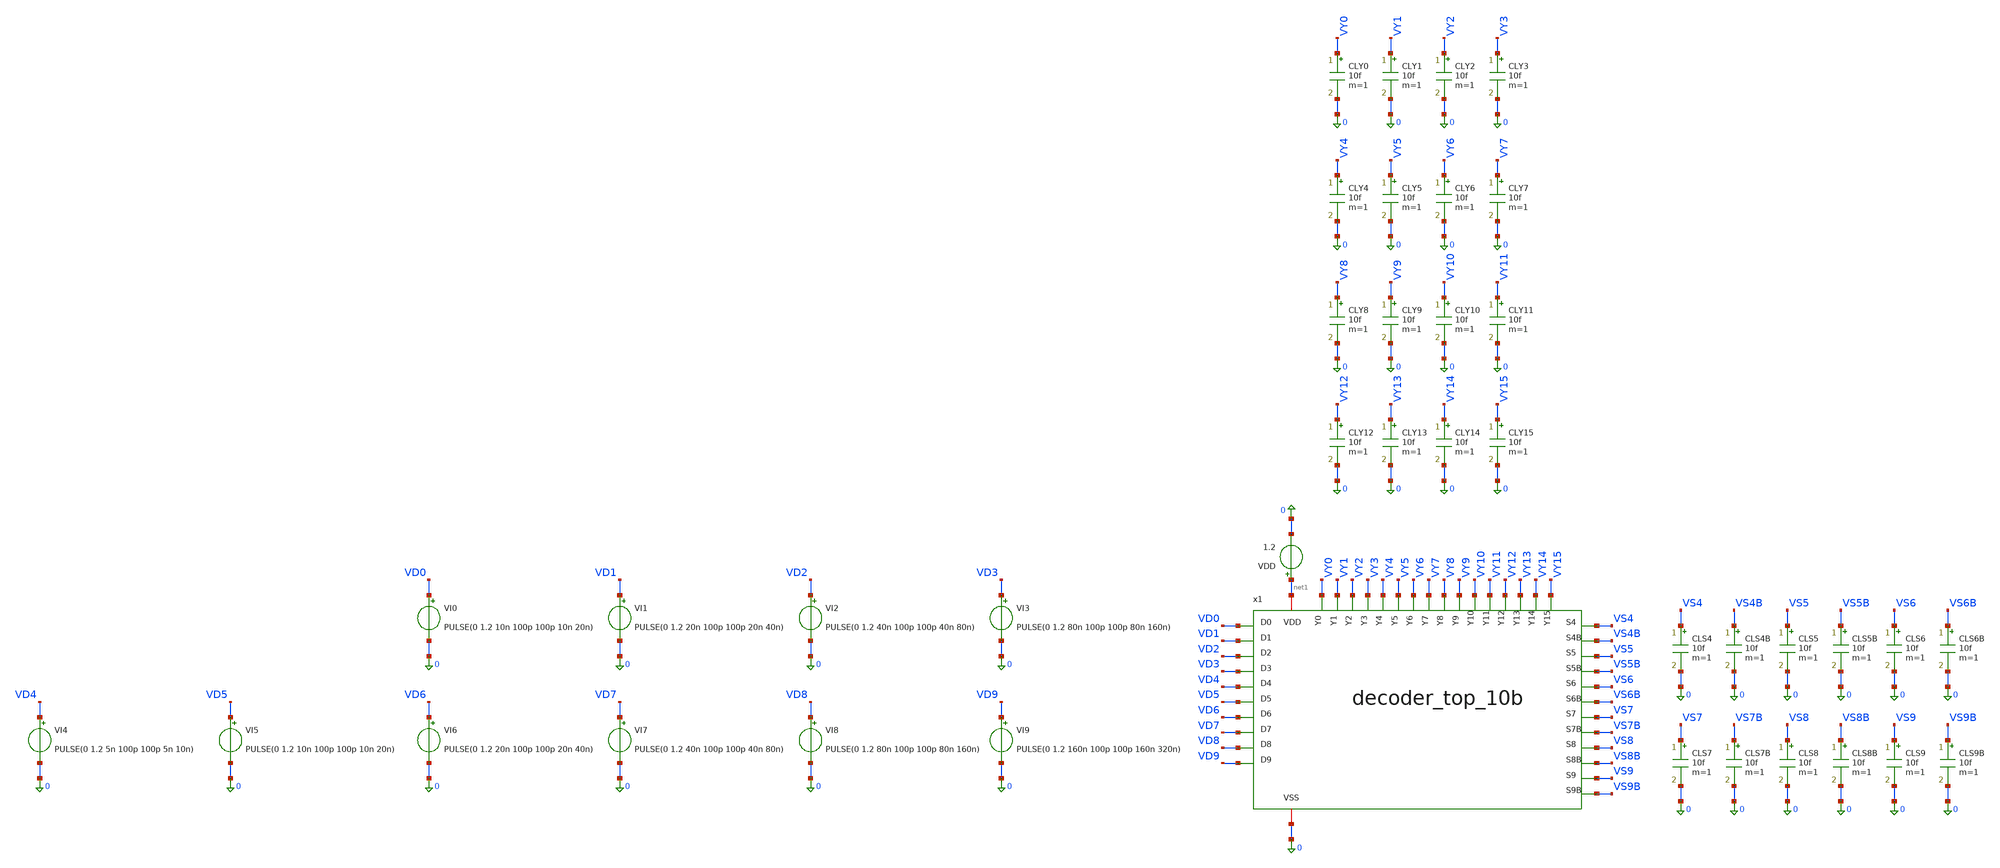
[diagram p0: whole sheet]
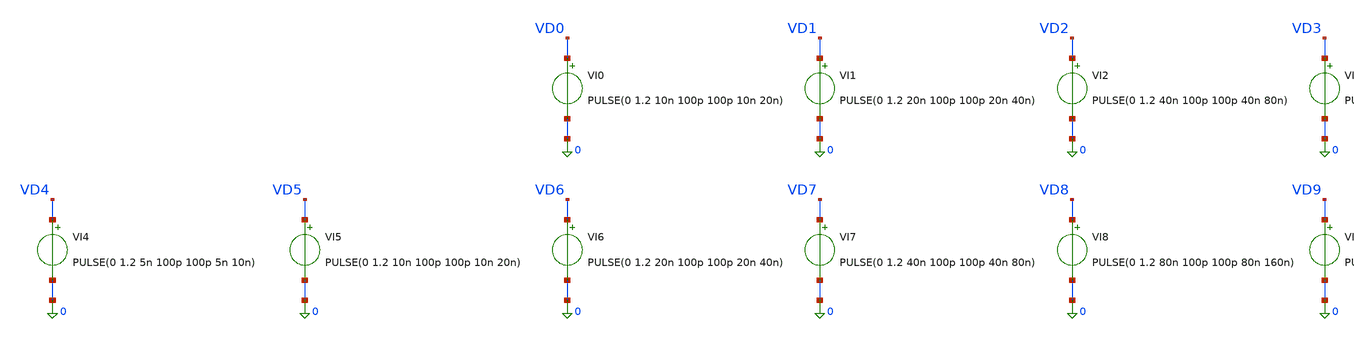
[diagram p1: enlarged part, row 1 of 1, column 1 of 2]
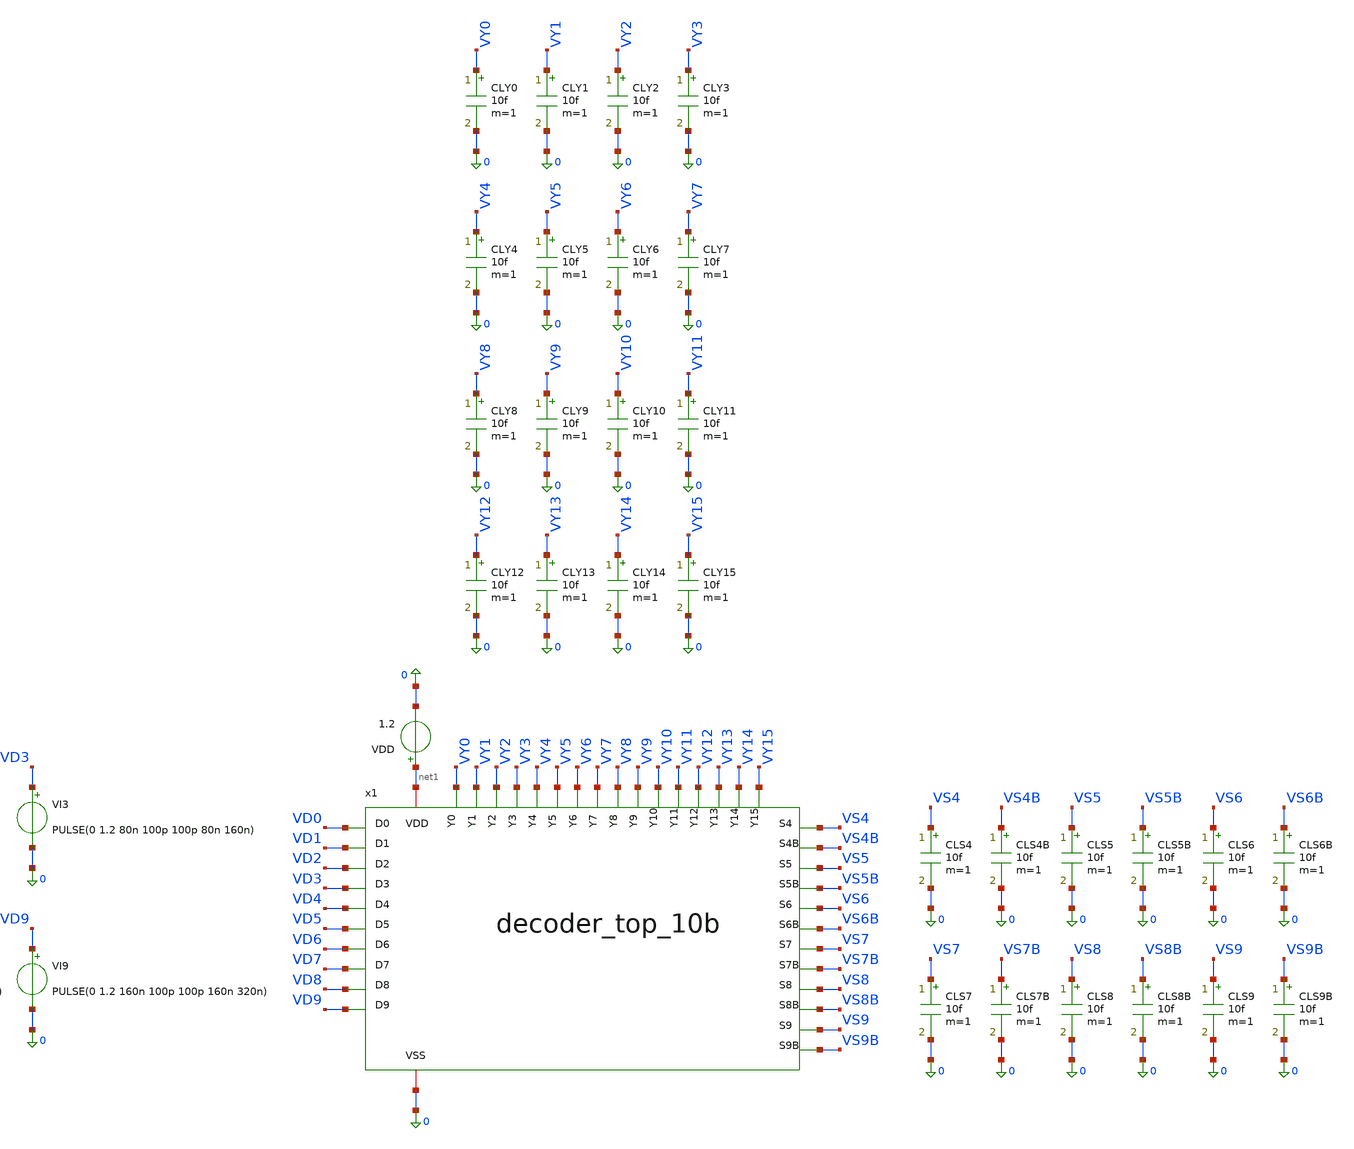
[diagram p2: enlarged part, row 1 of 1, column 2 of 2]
** sch_path: designs/archives/decoder_top_10b/tb_decoder_top_10b.sch
**.subckt tb_decoder_top_10b
x1 VD0 VD3 VY0 VY1 VY2 VY3 net1 0 VY4 VY5 VY6 VY7 VY8 VY9 VY10 VY11 VY12 VY13 VY14 VY15 VD1 VD2 VD4
+ VD7 VD5 VD6 VD8 VD9 VS4 VS4B VS5 VS5B VS6 VS6B VS7 VS7B VS8 VS8B VS9 VS9B decoder_top_10b
VDD net1 0 1.2
VI0 VD0 0 PULSE(0 1.2 10n 100p 100p 10n 20n)
VI1 VD1 0 PULSE(0 1.2 20n 100p 100p 20n 40n)
VI2 VD2 0 PULSE(0 1.2 40n 100p 100p 40n 80n)
VI3 VD3 0 PULSE(0 1.2 80n 100p 100p 80n 160n)
VI4 VD4 0 PULSE(0 1.2 5n 100p 100p 5n 10n)
VI5 VD5 0 PULSE(0 1.2 10n 100p 100p 10n 20n)
VI6 VD6 0 PULSE(0 1.2 20n 100p 100p 20n 40n)
VI7 VD7 0 PULSE(0 1.2 40n 100p 100p 40n 80n)
VI8 VD8 0 PULSE(0 1.2 80n 100p 100p 80n 160n)
VI9 VD9 0 PULSE(0 1.2 160n 100p 100p 160n 320n)
CLY0 VY0 0 10f m=1
CLY1 VY1 0 10f m=1
CLY2 VY2 0 10f m=1
CLY3 VY3 0 10f m=1
CLY4 VY4 0 10f m=1
CLY5 VY5 0 10f m=1
CLY6 VY6 0 10f m=1
CLY7 VY7 0 10f m=1
CLY8 VY8 0 10f m=1
CLY9 VY9 0 10f m=1
CLY10 VY10 0 10f m=1
CLY11 VY11 0 10f m=1
CLY12 VY12 0 10f m=1
CLY13 VY13 0 10f m=1
CLY14 VY14 0 10f m=1
CLY15 VY15 0 10f m=1
CLS4 VS4 0 10f m=1
CLS4B VS4B 0 10f m=1
CLS6B VS6B 0 10f m=1
CLS5B VS5B 0 10f m=1
CLS5 VS5 0 10f m=1
CLS6 VS6 0 10f m=1
CLS7 VS7 0 10f m=1
CLS7B VS7B 0 10f m=1
CLS8 VS8 0 10f m=1
CLS8B VS8B 0 10f m=1
CLS9 VS9 0 10f m=1
CLS9B VS9B 0 10f m=1
**** begin user architecture code

.lib cornerMOSlv.lib mos_tt
.include /foss/pdks/ihp-sg13cmos5l/libs.ref/sg13cmos5l_stdcell/spice/sg13cmos5l_stdcell.spice


.control
  tran 100p 320n
  write tb_decoder_top_10b.raw

  * ==========================================
  * 1. COARSE GAIN STAGE (D0..D3 -> Y0..Y15)
  * ==========================================
  * Coarse 4-bit Binary Inputs (D0..D3)
  plot v(VD0) v(VD1)+1.5 v(VD2)+3.0 v(VD3)+4.5 title 'Coarse Inputs (D0, D1, D2, D3)' xlabel 'Time (s)'
+ ylabel 'Voltage (V)'

  * Coarse Outputs Lower 8 Channels (Y0..Y7)
  plot v(VY0) v(VY1)+1.5 v(VY2)+3.0 v(VY3)+4.5 v(VY4)+6.0 v(VY5)+7.5 v(VY6)+9.0 v(VY7)+10.5 title 'Coarse Decoded Outputs (Y0..Y7)'
+ xlabel 'Time (s)' ylabel 'Voltage (V)'

  * Coarse Outputs Upper 8 Channels (Y8..Y15)
  plot v(VY8) v(VY9)+1.5 v(VY10)+3.0 v(VY11)+4.5 v(VY12)+6.0 v(VY13)+7.5 v(VY14)+9.0 v(VY15)+10.5 title
+ 'Coarse Decoded Outputs (Y8..Y15)' xlabel 'Time (s)' ylabel 'Voltage (V)'

  * ==========================================
  * 2. FINE GAIN STAGE (D4..D9 -> S4..S9B)
  * ==========================================
  * Fine 6-bit Inputs (D4..D9)
  plot v(VD4) v(VD5)+1.5 v(VD6)+3.0 v(VD7)+4.5 v(VD8)+6.0 v(VD9)+7.5 title 'Fine Inputs (D4, D5, D6, D7, D8, D9)'
+ xlabel 'Time (s)' ylabel 'Voltage (V)'

  * Fine Complementary Outputs: Bits 4 - 6 (S4/S4B, S5/S5B, S6/S6B)
  plot v(VS4) v(VS4B)+1.5 v(VS5)+3.0 v(VS5B)+4.5 v(VS6)+6.0 v(VS6B)+7.5 title 'Fine Driver Outputs (Bits 4-6)'
+ xlabel 'Time (s)' ylabel 'Voltage (V)'

  * Fine Complementary Outputs: Bits 7 - 9 (S7/S7B, S8/S8B, S9/S9B)
  plot v(VS7) v(VS7B)+1.5 v(VS8)+3.0 v(VS8B)+4.5 v(VS9)+6.0 v(VS9B)+7.5 title 'Fine Driver Outputs (Bits 7-9)'
+ xlabel 'Time (s)' ylabel 'Voltage (V)'
.endc

**** end user architecture code
**.ends
.end
